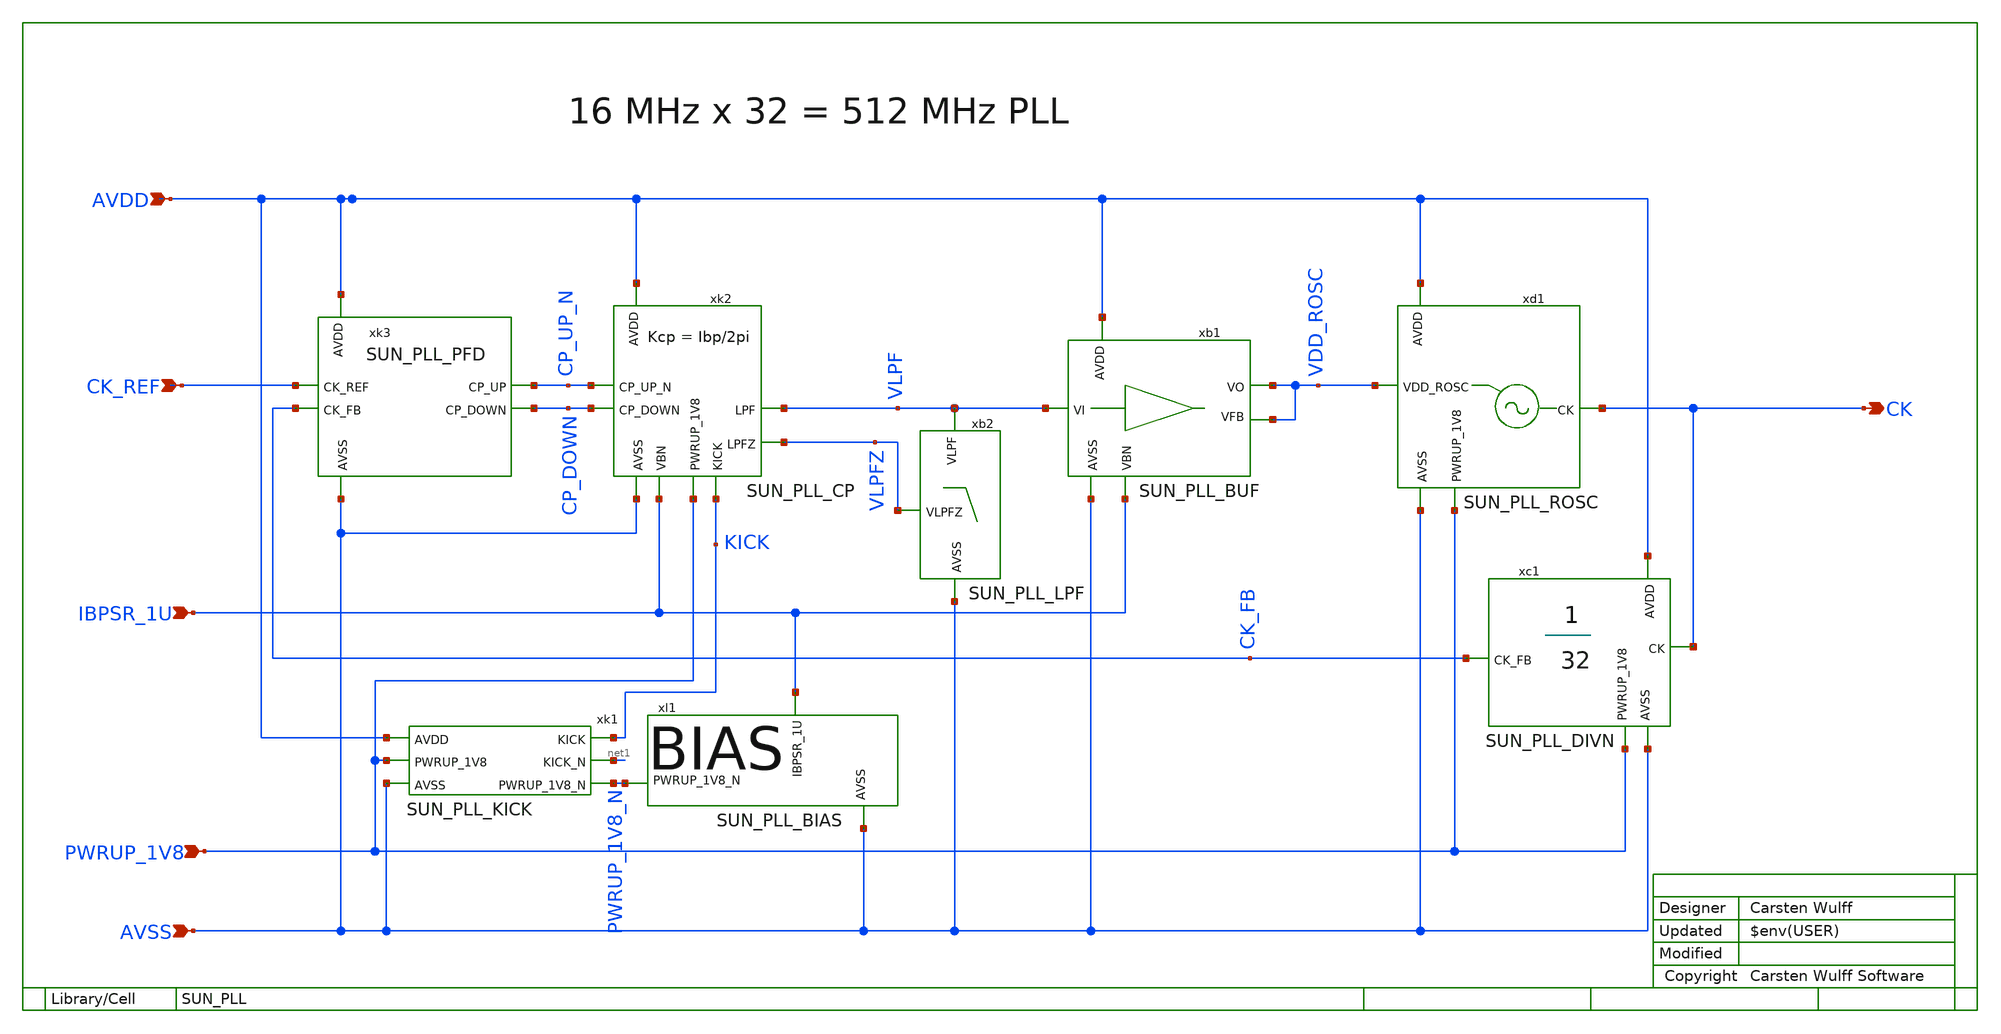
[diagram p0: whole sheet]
** sch_path: ip/sun_pll_sky130nm/design/SUN_PLL_SKY130NM/SUN_PLL.sch
**.subckt SUN_PLL AVDD AVSS PWRUP_1V8 CK_REF CK IBPSR_1U
*.ipin AVDD
*.ipin AVSS
*.ipin PWRUP_1V8
*.ipin CK_REF
*.opin CK
*.ipin IBPSR_1U
xd1 AVDD CK VDD_ROSC PWRUP_1V8 AVSS SUN_PLL_ROSC xoffset=5 yoffset=0 angle=0
xc1 AVDD CK_FB CK PWRUP_1V8 AVSS SUN_PLL_DIVN xoffset=-310 yoffset=0 angle=0
xl1 IBPSR_1U PWRUP_1V8_N AVSS SUN_PLL_BIAS xoffset=5 yoffset=0 angle=0
xb1 AVDD VDD_ROSC VLPF VDD_ROSC IBPSR_1U AVSS SUN_PLL_BUF xoffset=0 yoffset=0 angle=0
xb2 VLPFZ AVSS VLPF SUN_PLL_LPF xoffset=0 yoffset=5 angle=0
xk2 AVDD CP_UP_N VLPF CP_DOWN IBPSR_1U AVSS VLPFZ PWRUP_1V8 KICK SUN_PLL_CP xoffset=0 yoffset=5
+ angle=0
xk3 AVDD CP_UP_N CK_REF CP_DOWN CK_FB AVSS SUN_PLL_PFD
xk1 AVDD KICK net1 PWRUP_1V8 AVSS PWRUP_1V8_N SUN_PLL_KICK xoffset=20 yoffset=0 angle=0
**.ends
.end
